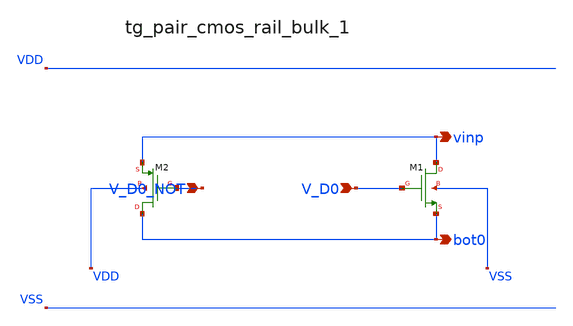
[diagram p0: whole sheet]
** sch_path: analog-db/raw/sw_003_binary_capbank/hier/blocks/tg_pair_cmos_rail_bulk_1.sch
**.subckt tg_pair_cmos_rail_bulk_1 V_D0_NOT V_D0 vinp bot0
*.ipin V_D0_NOT
*.ipin V_D0
*.opin vinp
*.opin bot0
XM1 vinp V_D0 bot0 VSS sg13_lv_nmos w=x_dut_xm1_w l=x_dut_xm1_l ng=1 m=x_dut_xm1_m
XM2 bot0 V_D0_NOT vinp VDD sg13_lv_pmos w=x_dut_xm2_w l=x_dut_xm2_l ng=1 m=x_dut_xm2_m
**.ends
.end
